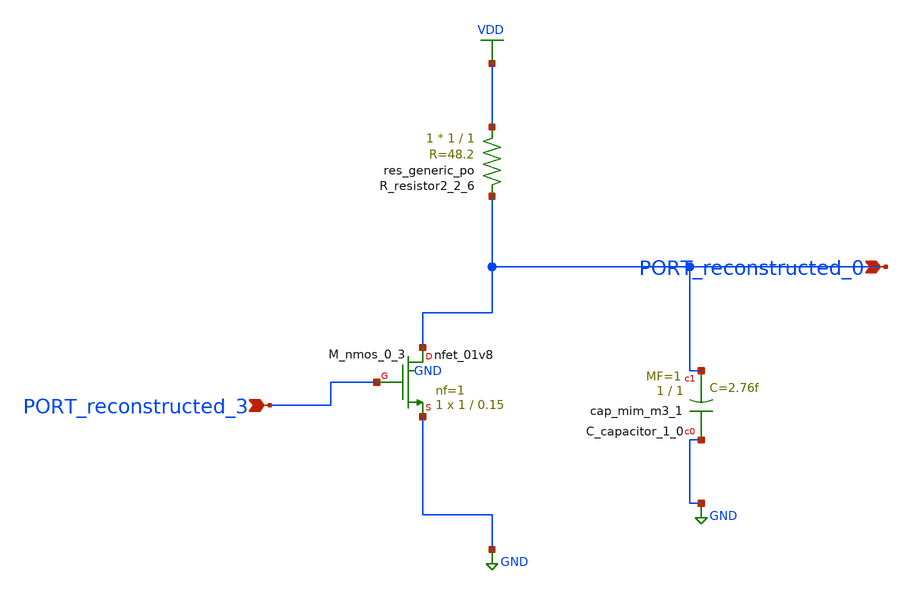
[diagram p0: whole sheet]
** sch_path: schematics/AMSNet/463.sch
**.subckt 463 PORT_reconstructed_3 PORT_reconstructed_0
*.ipin PORT_reconstructed_3
*.ipin PORT_reconstructed_0
XC_capacitor_1_0 GND PORT_reconstructed_0 sky130_fd_pr__cap_mim_m3_1 W=1 L=1 MF=1 m=1
XM_nmos_0_3 PORT_reconstructed_0 PORT_reconstructed_3 GND GND sky130_fd_pr__nfet_01v8 L=0.15 W=1 nf=1
+ ad='int((1 + 1)/2) * 1 / 1 * 0.29' as='int((1 + 2)/2) * 1 / 1 * 0.29' pd='2*int((1 + 1)/2) * (1 / 1 + 0.29)'
+ ps='2*int((1 + 2)/2) * (1 / 1 + 0.29)' nrd='0.29 / 1 ' nrs='0.29 / 1 ' sa=0 sb=0 sd=0 mult=1 m=1
XR_resistor2_2_6 VDD PORT_reconstructed_0 sky130_fd_pr__res_generic_po W=1 L=1 m=1
**.ends
.GLOBAL GND
.GLOBAL VDD
.end
